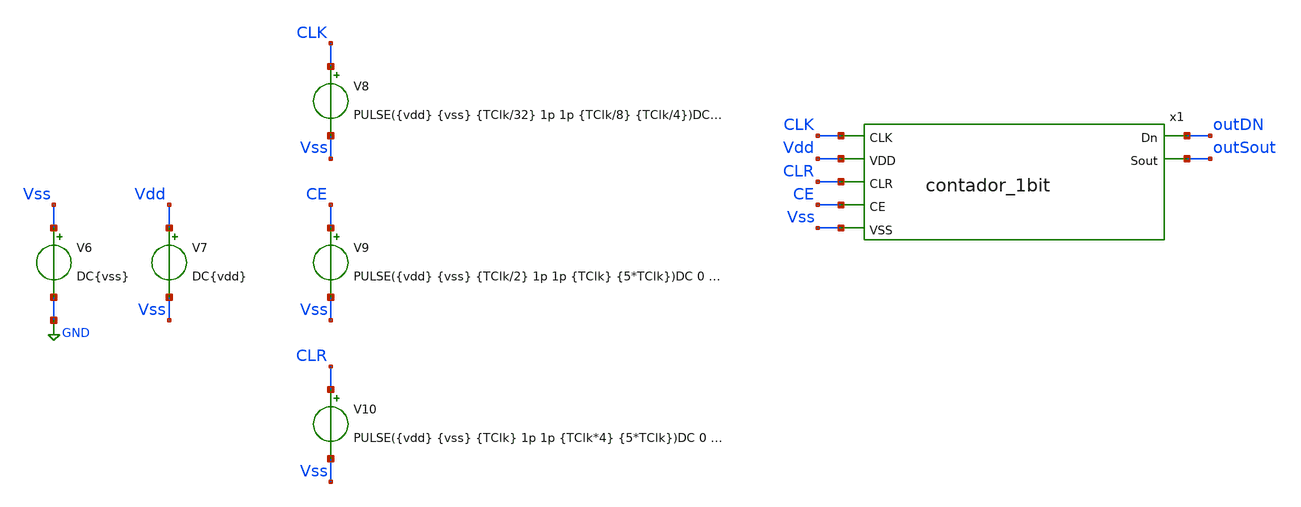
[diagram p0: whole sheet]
** sch_path: icdesign/sch/Contador1bit/tb_contador_1bit.sch
**.subckt tb_contador_1bit
x1 outDN CLK Vdd CLR CE Vss outSout contador_1bit
V6 Vss GND DC{vss}
V7 Vdd Vss DC{vdd}
V8 CLK Vss PULSE({vdd} {vss} {TClk/32} 1p 1p {TClk/8} {TClk/4})DC 0 AC 0
V9 CE Vss PULSE({vdd} {vss} {TClk/2} 1p 1p {TClk} {5*TClk})DC 0 AC 0
V10 CLR Vss PULSE({vdd} {vss} {TClk} 1p 1p {TClk*4} {5*TClk})DC 0 AC 0
**** begin user architecture code





* Circuit Parameters
.param vdd  = 1.8
.param vss  = 0.0
.param Tclk = 10n
.options TEMP = 65.0


* Include Models
.lib ~/skywater/skywater-pdk/libraries/sky130_fd_pr_ngspice/latest/models/corners/sky130.lib TT


* OP Parameters & Singals to save
.save all


*Simulations
.control
  tran 0.01u 50n
  setplot tran1
  plot v(CLK)v(CLR)+2 v(CE)+4 v(outDN)+6 v(outSout)+8
.endc
.end


**** end user architecture code
**.ends
.GLOBAL GND
.end
